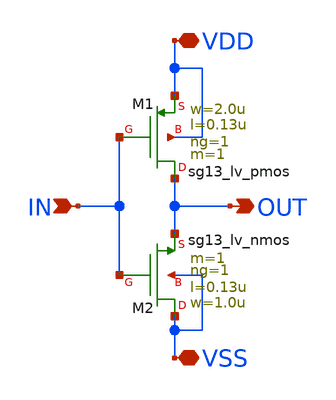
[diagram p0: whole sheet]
** sch_path: designs/1iee34/inv_1x.sch
**.subckt inv_1x VDD VSS IN OUT
*.iopin VDD
*.iopin VSS
*.ipin IN
*.opin OUT
XM1 OUT IN VDD VDD sg13_lv_pmos w=2.0u l=0.13u ng=1 m=1 mm_ok=1
XM2 VSS IN OUT VSS sg13_lv_nmos w=1.0u l=0.13u ng=1 m=1 mm_ok=1
**.ends
.end
